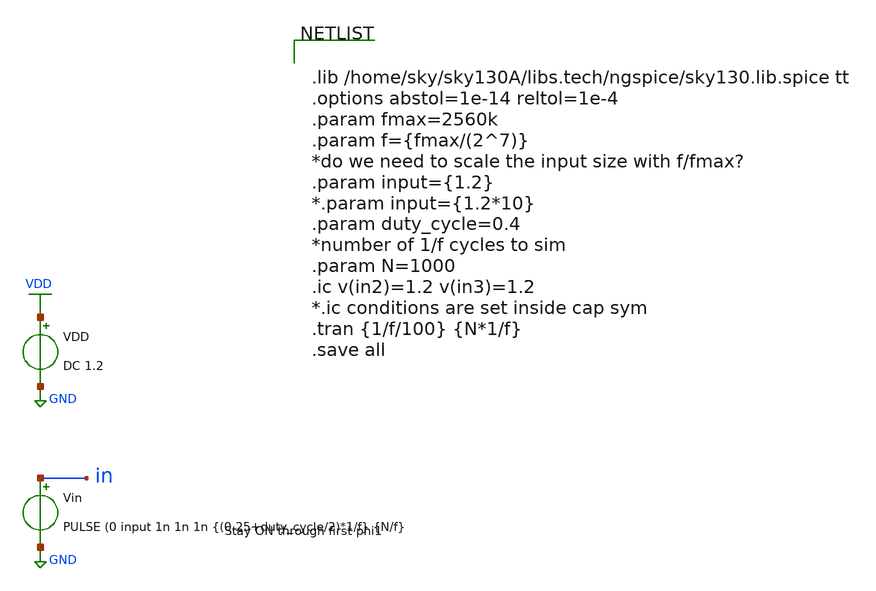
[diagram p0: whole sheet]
** sch_path: xschem/Switched_Caps/lpf_gmC_tb.sch
**.subckt lpf_gmC_tb
Vin in GND PULSE (0 input 1n 1n 1n {(0.25+duty_cycle/2)*1/f} {N/f}
VDD VDD GND DC 1.2
**** begin user architecture code


.lib /home/sky/sky130A/libs.tech/ngspice/sky130.lib.spice tt
.options abstol=1e-14 reltol=1e-4
.param fmax=2560k
.param f={fmax/(2^7)}
*do we need to scale the input size with f/fmax?
.param input={1.2}
*.param input={1.2*10}
.param duty_cycle=0.4
*number of 1/f cycles to sim
.param N=1000
.ic v(in2)=1.2 v(in3)=1.2
*.ic conditions are set inside cap sym
.tran {1/f/100} {N*1/f}
.save all


**** end user architecture code
**.ends
.GLOBAL GND
.GLOBAL VDD
.end
